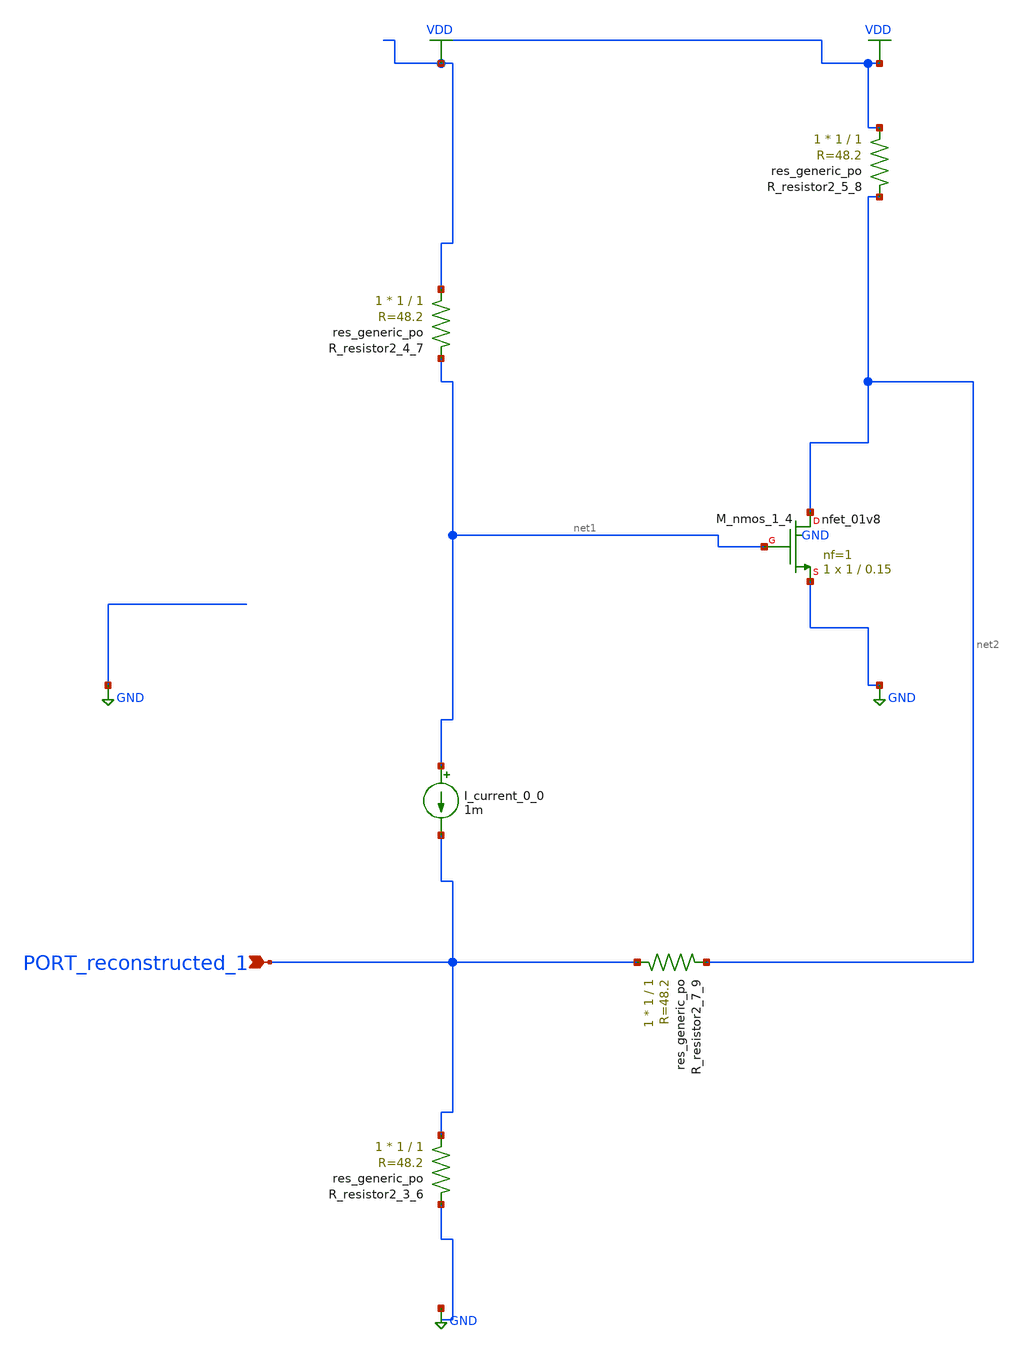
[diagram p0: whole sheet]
** sch_path: schematics/AMSNet/601.sch
**.subckt 601 PORT_reconstructed_1
*.ipin PORT_reconstructed_1
I_current_0_0 net1 PORT_reconstructed_1 1m
XM_nmos_1_4 net2 net1 GND GND sky130_fd_pr__nfet_01v8 L=0.15 W=1 nf=1 ad='int((1 + 1)/2) * 1 / 1 * 0.29'
+ as='int((1 + 2)/2) * 1 / 1 * 0.29' pd='2*int((1 + 1)/2) * (1 / 1 + 0.29)' ps='2*int((1 + 2)/2) * (1 / 1 + 0.29)'
+ nrd='0.29 / 1 ' nrs='0.29 / 1 ' sa=0 sb=0 sd=0 mult=1 m=1
XR_resistor2_3_6 PORT_reconstructed_1 GND sky130_fd_pr__res_generic_po W=1 L=1 m=1
XR_resistor2_4_7 VDD net1 sky130_fd_pr__res_generic_po W=1 L=1 m=1
XR_resistor2_5_8 VDD net2 sky130_fd_pr__res_generic_po W=1 L=1 m=1
XR_resistor2_7_9 PORT_reconstructed_1 net2 sky130_fd_pr__res_generic_po W=1 L=1 m=1
**.ends
.GLOBAL GND
.GLOBAL VDD
.end
